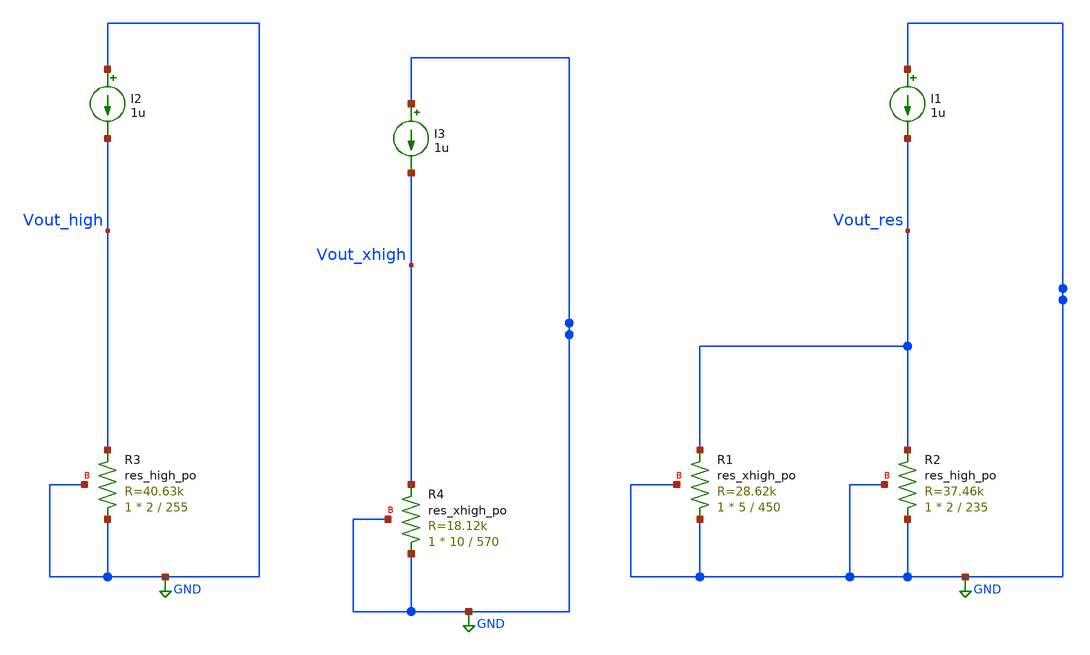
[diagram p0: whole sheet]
** sch_path: design/misc/testing/res_current_ref_para.sch
**.subckt res_current_ref_para
I1 GND Vout_res 1u
XR2 GND Vout_res GND sky130_fd_pr__res_high_po W=2 L=235 mult=1 m=1
XR1 GND Vout_res GND sky130_fd_pr__res_xhigh_po W=5 L=450 mult=1 m=1
I2 GND Vout_high 1u
XR3 GND Vout_high GND sky130_fd_pr__res_high_po W=2 L=255 mult=1 m=1
I3 GND Vout_xhigh 1u
XR4 GND Vout_xhigh GND sky130_fd_pr__res_xhigh_po W=10 L=570 mult=1 m=1
**** begin user architecture code
.lib $::SKYWATER_MODELS/sky130.lib.spice tt


.param temp=27

.dc temp -20 100 1


.save all
.control
run
plot Vout_res
plot deriv(Vout_res)
plot Vout_high
plot deriv(Vout_high)
plot Vout_xhigh
plot deriv(Vout_xhigh)
let Rcomb = Vout_high*Vout_xhigh/(Vout_high + Vout_xhigh)
plot Rcomb
let Isim = 1.2/Rcomb
plot Isim
let Rnom = Vout_high*Vout_xhigh
let Rdim = Vout_high + Vout_xhigh
plot Rnom
plot Rdim

.endc



**** end user architecture code
**.ends
.GLOBAL GND
.end
